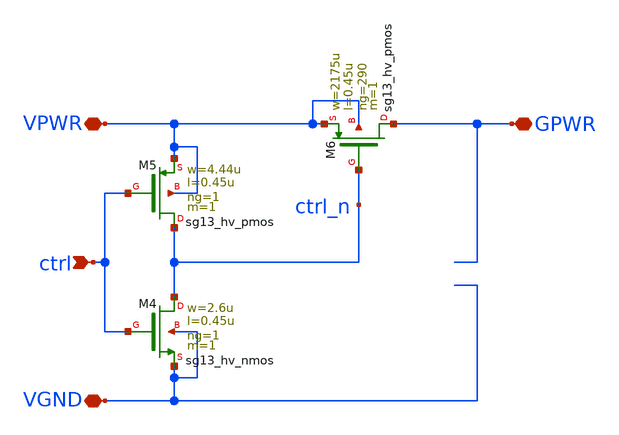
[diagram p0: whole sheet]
** sch_path: ihp-sg13cmos5l/libs.tech/xschem/hm_analog/hm_pg_hv.sch
**.subckt hm_pg_hv ctrl VPWR VGND GPWR
*.ipin ctrl
*.iopin VPWR
*.iopin VGND
*.iopin GPWR
XM4 ctrl_n ctrl VGND VGND sg13_hv_nmos w=2.6u l=0.45u ng=1 m=1 mm_ok=1
XM5 ctrl_n ctrl VPWR VPWR sg13_hv_pmos w=4.44u l=0.45u ng=1 m=1 mm_ok=1
XM6 GPWR ctrl_n VPWR VPWR sg13_hv_pmos w=2175u l=0.45u ng=290 m=1 mm_ok=1
**.ends
.end
